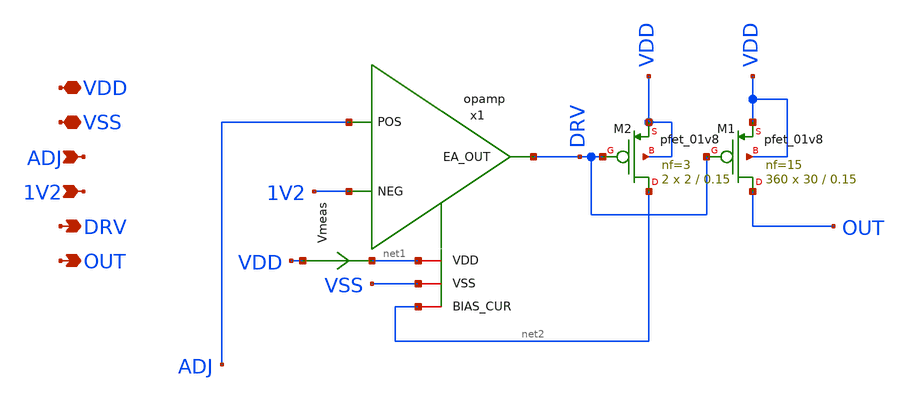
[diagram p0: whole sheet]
** sch_path: xschem/ab_ldo.sch
**.subckt ab_ldo VDD VSS ADJ 1V2 DRV OUT
*.iopin VDD
*.iopin VSS
*.ipin ADJ
*.ipin 1V2
*.opin DRV
*.opin OUT
x1 ADJ 1V2 VSS net1 DRV net2 opamp
XM1 OUT DRV VDD VDD sky130_fd_pr__pfet_01v8 L=0.15 W=30 nf=15 ad='int((nf+1)/2) * W/nf * 0.29' as='int((nf+2)/2) * W/nf * 0.29'
+ pd='2*int((nf+1)/2) * (W/nf + 0.29)' ps='2*int((nf+2)/2) * (W/nf + 0.29)' nrd='0.29 / W' nrs='0.29 / W'
+ sa=0 sb=0 sd=0 mult=360 m=360
Vmeas VDD net1 0
.save i(vmeas)
XM2 net2 DRV VDD VDD sky130_fd_pr__pfet_01v8 L=0.15 W=2 nf=3 ad='int((nf+1)/2) * W/nf * 0.29' as='int((nf+2)/2) * W/nf * 0.29'
+ pd='2*int((nf+1)/2) * (W/nf + 0.29)' ps='2*int((nf+2)/2) * (W/nf + 0.29)' nrd='0.29 / W' nrs='0.29 / W'
+ sa=0 sb=0 sd=0 mult=2 m=2
**.ends

* expanding   symbol:  opamp.sym # of pins=6
** sym_path: xschem/opamp.sym
** sch_path: xschem/opamp.sch
.subckt opamp POS NEG VSS VDD EA_OUT BIAS_CUR
*.ipin POS
*.ipin NEG
*.iopin VDD
*.iopin VSS
*.ipin BIAS_CUR
*.opin EA_OUT
XM3 POS_D POS_D VDD VDD sky130_fd_pr__pfet_01v8 L=0.3 W=5 nf=1 ad='int((nf+1)/2) * W/nf * 0.29' as='int((nf+2)/2) * W/nf * 0.29'
+ pd='2*int((nf+1)/2) * (W/nf + 0.29)' ps='2*int((nf+2)/2) * (W/nf + 0.29)' nrd='0.29 / W' nrs='0.29 / W'
+ sa=0 sb=0 sd=0 mult=4 m=4
XM4 NEG_D NEG_D VDD VDD sky130_fd_pr__pfet_01v8 L=0.3 W=5 nf=1 ad='int((nf+1)/2) * W/nf * 0.29' as='int((nf+2)/2) * W/nf * 0.29'
+ pd='2*int((nf+1)/2) * (W/nf + 0.29)' ps='2*int((nf+2)/2) * (W/nf + 0.29)' nrd='0.29 / W' nrs='0.29 / W'
+ sa=0 sb=0 sd=0 mult=4 m=4
XM5 NEG_2 NEG_D VDD VDD sky130_fd_pr__pfet_01v8 L=0.3 W=5 nf=1 ad='int((nf+1)/2) * W/nf * 0.29' as='int((nf+2)/2) * W/nf * 0.29'
+ pd='2*int((nf+1)/2) * (W/nf + 0.29)' ps='2*int((nf+2)/2) * (W/nf + 0.29)' nrd='0.29 / W' nrs='0.29 / W'
+ sa=0 sb=0 sd=0 mult=8 m=8
XM7 EA_OUT POS_D VDD VDD sky130_fd_pr__pfet_01v8 L=0.3 W=5 nf=1 ad='int((nf+1)/2) * W/nf * 0.29' as='int((nf+2)/2) * W/nf * 0.29'
+ pd='2*int((nf+1)/2) * (W/nf + 0.29)' ps='2*int((nf+2)/2) * (W/nf + 0.29)' nrd='0.29 / W' nrs='0.29 / W'
+ sa=0 sb=0 sd=0 mult=8 m=8
XM9 NEG_D NEG P1 VSS sky130_fd_pr__nfet_01v8 L=0.5 W=4 nf=1 ad='int((nf+1)/2) * W/nf * 0.29' as='int((nf+2)/2) * W/nf * 0.29'
+ pd='2*int((nf+1)/2) * (W/nf + 0.29)' ps='2*int((nf+2)/2) * (W/nf + 0.29)' nrd='0.29 / W' nrs='0.29 / W'
+ sa=0 sb=0 sd=0 mult=8 m=8
XM10 POS_D POS P1 VSS sky130_fd_pr__nfet_01v8 L=0.5 W=4 nf=1 ad='int((nf+1)/2) * W/nf * 0.29' as='int((nf+2)/2) * W/nf * 0.29'
+ pd='2*int((nf+1)/2) * (W/nf + 0.29)' ps='2*int((nf+2)/2) * (W/nf + 0.29)' nrd='0.29 / W' nrs='0.29 / W'
+ sa=0 sb=0 sd=0 mult=8 m=8
XM11 BIAS_CUR BIAS_CUR VSS VSS sky130_fd_pr__nfet_01v8 L=1 W=2.5 nf=1 ad='int((nf+1)/2) * W/nf * 0.29'
+ as='int((nf+2)/2) * W/nf * 0.29' pd='2*int((nf+1)/2) * (W/nf + 0.29)' ps='2*int((nf+2)/2) * (W/nf + 0.29)'
+ nrd='0.29 / W' nrs='0.29 / W' sa=0 sb=0 sd=0 mult=16 m=16
XM12 P1 BIAS_CUR VSS VSS sky130_fd_pr__nfet_01v8 L=1 W=2.5 nf=1 ad='int((nf+1)/2) * W/nf * 0.29' as='int((nf+2)/2) * W/nf * 0.29'
+ pd='2*int((nf+1)/2) * (W/nf + 0.29)' ps='2*int((nf+2)/2) * (W/nf + 0.29)' nrd='0.29 / W' nrs='0.29 / W'
+ sa=0 sb=0 sd=0 mult=16 m=16
XM13 NEG_2 NEG_2 VSS VSS sky130_fd_pr__nfet_01v8 L=0.3 W=10 nf=2 ad='int((nf+1)/2) * W/nf * 0.29' as='int((nf+2)/2) * W/nf * 0.29'
+ pd='2*int((nf+1)/2) * (W/nf + 0.29)' ps='2*int((nf+2)/2) * (W/nf + 0.29)' nrd='0.29 / W' nrs='0.29 / W'
+ sa=0 sb=0 sd=0 mult=5 m=5
XM1 P1 VSS VSS VSS sky130_fd_pr__nfet_01v8_lvt L=0.15 W=200 nf=20 ad='int((nf+1)/2) * W/nf * 0.29' as='int((nf+2)/2) * W/nf * 0.29'
+ pd='2*int((nf+1)/2) * (W/nf + 0.29)' ps='2*int((nf+2)/2) * (W/nf + 0.29)' nrd='0.29 / W' nrs='0.29 / W'
+ sa=0 sb=0 sd=0 mult=15 m=15
XM2 EA_OUT NEG_2 VSS VSS sky130_fd_pr__nfet_01v8 L=0.3 W=10 nf=2 ad='int((nf+1)/2) * W/nf * 0.29' as='int((nf+2)/2) * W/nf * 0.29'
+ pd='2*int((nf+1)/2) * (W/nf + 0.29)' ps='2*int((nf+2)/2) * (W/nf + 0.29)' nrd='0.29 / W' nrs='0.29 / W'
+ sa=0 sb=0 sd=0 mult=5 m=5
XM6 P1 VSS VSS VSS sky130_fd_pr__nfet_01v8 L=1 W=2.5 nf=1 ad='int((nf+1)/2) * W/nf * 0.29' as='int((nf+2)/2) * W/nf * 0.29'
+ pd='2*int((nf+1)/2) * (W/nf + 0.29)' ps='2*int((nf+2)/2) * (W/nf + 0.29)' nrd='0.29 / W' nrs='0.29 / W'
+ sa=0 sb=0 sd=0 mult=2 m=2
XM8 NEG_D P1 P1 VSS sky130_fd_pr__nfet_01v8 L=0.5 W=4 nf=1 ad='int((nf+1)/2) * W/nf * 0.29' as='int((nf+2)/2) * W/nf * 0.29'
+ pd='2*int((nf+1)/2) * (W/nf + 0.29)' ps='2*int((nf+2)/2) * (W/nf + 0.29)' nrd='0.29 / W' nrs='0.29 / W'
+ sa=0 sb=0 sd=0 mult=2 m=2
XM14 NEG_D VDD VDD VDD sky130_fd_pr__pfet_01v8 L=0.3 W=5 nf=1 ad='int((nf+1)/2) * W/nf * 0.29' as='int((nf+2)/2) * W/nf * 0.29'
+ pd='2*int((nf+1)/2) * (W/nf + 0.29)' ps='2*int((nf+2)/2) * (W/nf + 0.29)' nrd='0.29 / W' nrs='0.29 / W'
+ sa=0 sb=0 sd=0 mult=4 m=4
XM15 POS_D VDD VDD VDD sky130_fd_pr__pfet_01v8 L=0.3 W=5 nf=1 ad='int((nf+1)/2) * W/nf * 0.29' as='int((nf+2)/2) * W/nf * 0.29'
+ pd='2*int((nf+1)/2) * (W/nf + 0.29)' ps='2*int((nf+2)/2) * (W/nf + 0.29)' nrd='0.29 / W' nrs='0.29 / W'
+ sa=0 sb=0 sd=0 mult=4 m=4
.ends

.end
